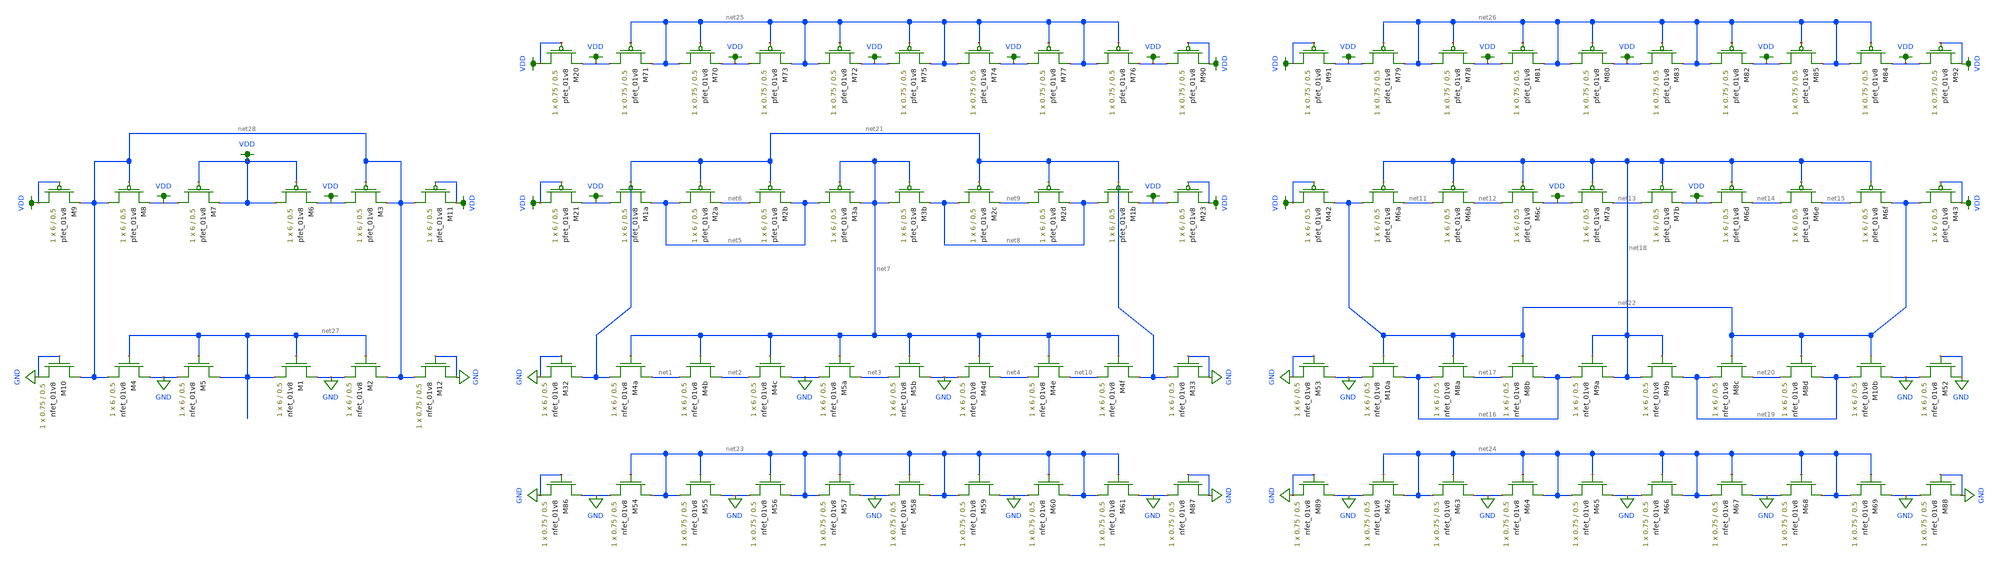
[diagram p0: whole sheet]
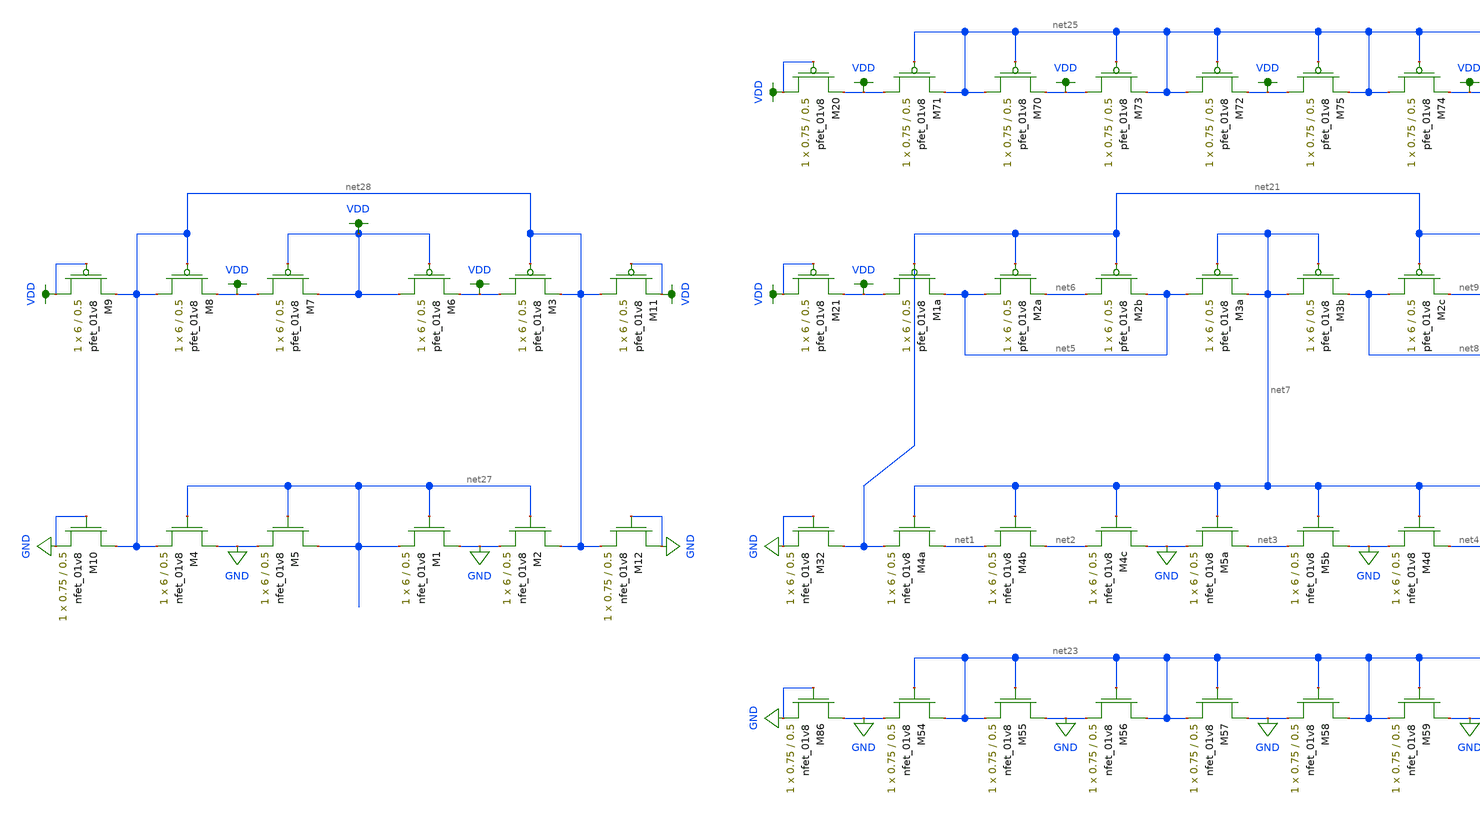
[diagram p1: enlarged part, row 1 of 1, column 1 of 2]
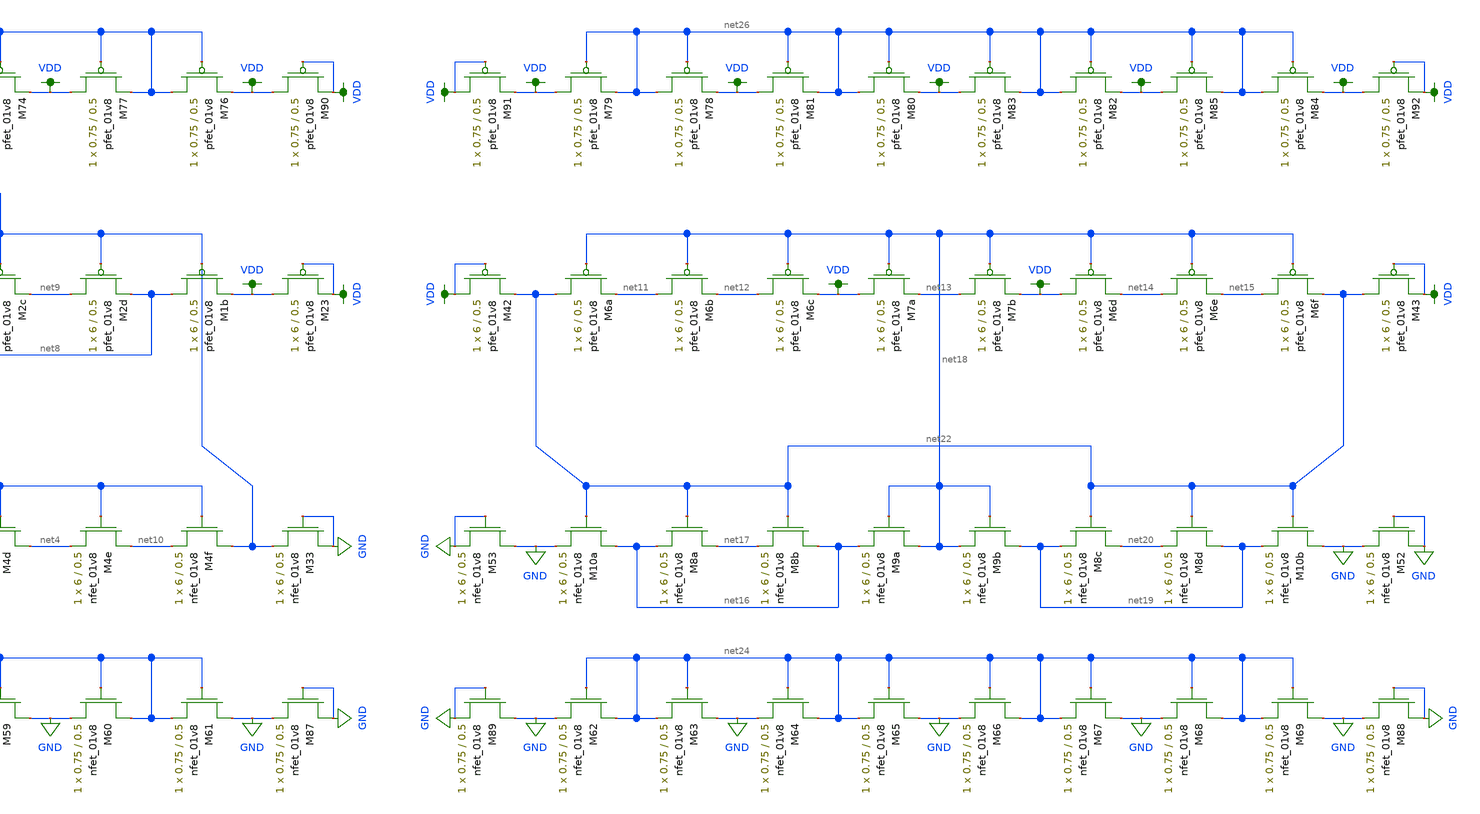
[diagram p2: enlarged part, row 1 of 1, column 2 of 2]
** sch_path: mini3/schem/bias_lvs.sch
**.subckt bias_lvs
XM4a net1 net7 net21 GND sky130_fd_pr__nfet_01v8 L=0.5 W=6 nf=1 ad='int((nf+1)/2) * W/nf * 0.29' as='int((nf+2)/2) * W/nf * 0.29'
+ pd='2*int((nf+1)/2) * (W/nf + 0.29)' ps='2*int((nf+2)/2) * (W/nf + 0.29)' nrd='0.29 / W' nrs='0.29 / W'
+ sa=0 sb=0 sd=0 mult=1 m=1
XM4b net2 net7 net1 GND sky130_fd_pr__nfet_01v8 L=0.5 W=6 nf=1 ad='int((nf+1)/2) * W/nf * 0.29' as='int((nf+2)/2) * W/nf * 0.29'
+ pd='2*int((nf+1)/2) * (W/nf + 0.29)' ps='2*int((nf+2)/2) * (W/nf + 0.29)' nrd='0.29 / W' nrs='0.29 / W'
+ sa=0 sb=0 sd=0 mult=1 m=1
XM4c GND net7 net2 GND sky130_fd_pr__nfet_01v8 L=0.5 W=6 nf=1 ad='int((nf+1)/2) * W/nf * 0.29' as='int((nf+2)/2) * W/nf * 0.29'
+ pd='2*int((nf+1)/2) * (W/nf + 0.29)' ps='2*int((nf+2)/2) * (W/nf + 0.29)' nrd='0.29 / W' nrs='0.29 / W'
+ sa=0 sb=0 sd=0 mult=1 m=1
XM5a net3 net7 GND GND sky130_fd_pr__nfet_01v8 L=0.5 W=6 nf=1 ad='int((nf+1)/2) * W/nf * 0.29' as='int((nf+2)/2) * W/nf * 0.29'
+ pd='2*int((nf+1)/2) * (W/nf + 0.29)' ps='2*int((nf+2)/2) * (W/nf + 0.29)' nrd='0.29 / W' nrs='0.29 / W'
+ sa=0 sb=0 sd=0 mult=1 m=1
XM5b GND net7 net3 GND sky130_fd_pr__nfet_01v8 L=0.5 W=6 nf=1 ad='int((nf+1)/2) * W/nf * 0.29' as='int((nf+2)/2) * W/nf * 0.29'
+ pd='2*int((nf+1)/2) * (W/nf + 0.29)' ps='2*int((nf+2)/2) * (W/nf + 0.29)' nrd='0.29 / W' nrs='0.29 / W'
+ sa=0 sb=0 sd=0 mult=1 m=1
XM4d net4 net7 GND GND sky130_fd_pr__nfet_01v8 L=0.5 W=6 nf=1 ad='int((nf+1)/2) * W/nf * 0.29' as='int((nf+2)/2) * W/nf * 0.29'
+ pd='2*int((nf+1)/2) * (W/nf + 0.29)' ps='2*int((nf+2)/2) * (W/nf + 0.29)' nrd='0.29 / W' nrs='0.29 / W'
+ sa=0 sb=0 sd=0 mult=1 m=1
XM4e net10 net7 net4 GND sky130_fd_pr__nfet_01v8 L=0.5 W=6 nf=1 ad='int((nf+1)/2) * W/nf * 0.29' as='int((nf+2)/2) * W/nf * 0.29'
+ pd='2*int((nf+1)/2) * (W/nf + 0.29)' ps='2*int((nf+2)/2) * (W/nf + 0.29)' nrd='0.29 / W' nrs='0.29 / W'
+ sa=0 sb=0 sd=0 mult=1 m=1
XM4f net21 net7 net10 GND sky130_fd_pr__nfet_01v8 L=0.5 W=6 nf=1 ad='int((nf+1)/2) * W/nf * 0.29' as='int((nf+2)/2) * W/nf * 0.29'
+ pd='2*int((nf+1)/2) * (W/nf + 0.29)' ps='2*int((nf+2)/2) * (W/nf + 0.29)' nrd='0.29 / W' nrs='0.29 / W'
+ sa=0 sb=0 sd=0 mult=1 m=1
XM1a VDD net21 net5 VDD sky130_fd_pr__pfet_01v8 L=0.5 W=6 nf=1 ad='int((nf+1)/2) * W/nf * 0.29' as='int((nf+2)/2) * W/nf * 0.29'
+ pd='2*int((nf+1)/2) * (W/nf + 0.29)' ps='2*int((nf+2)/2) * (W/nf + 0.29)' nrd='0.29 / W' nrs='0.29 / W'
+ sa=0 sb=0 sd=0 mult=1 m=1
XM2a net5 net21 net6 VDD sky130_fd_pr__pfet_01v8 L=0.5 W=6 nf=1 ad='int((nf+1)/2) * W/nf * 0.29' as='int((nf+2)/2) * W/nf * 0.29'
+ pd='2*int((nf+1)/2) * (W/nf + 0.29)' ps='2*int((nf+2)/2) * (W/nf + 0.29)' nrd='0.29 / W' nrs='0.29 / W'
+ sa=0 sb=0 sd=0 mult=1 m=1
XM2b net6 net21 net5 VDD sky130_fd_pr__pfet_01v8 L=0.5 W=6 nf=1 ad='int((nf+1)/2) * W/nf * 0.29' as='int((nf+2)/2) * W/nf * 0.29'
+ pd='2*int((nf+1)/2) * (W/nf + 0.29)' ps='2*int((nf+2)/2) * (W/nf + 0.29)' nrd='0.29 / W' nrs='0.29 / W'
+ sa=0 sb=0 sd=0 mult=1 m=1
XM3a net5 net7 net7 VDD sky130_fd_pr__pfet_01v8 L=0.5 W=6 nf=1 ad='int((nf+1)/2) * W/nf * 0.29' as='int((nf+2)/2) * W/nf * 0.29'
+ pd='2*int((nf+1)/2) * (W/nf + 0.29)' ps='2*int((nf+2)/2) * (W/nf + 0.29)' nrd='0.29 / W' nrs='0.29 / W'
+ sa=0 sb=0 sd=0 mult=1 m=1
XM3b net7 net7 net8 VDD sky130_fd_pr__pfet_01v8 L=0.5 W=6 nf=1 ad='int((nf+1)/2) * W/nf * 0.29' as='int((nf+2)/2) * W/nf * 0.29'
+ pd='2*int((nf+1)/2) * (W/nf + 0.29)' ps='2*int((nf+2)/2) * (W/nf + 0.29)' nrd='0.29 / W' nrs='0.29 / W'
+ sa=0 sb=0 sd=0 mult=1 m=1
XM2c net8 net21 net9 VDD sky130_fd_pr__pfet_01v8 L=0.5 W=6 nf=1 ad='int((nf+1)/2) * W/nf * 0.29' as='int((nf+2)/2) * W/nf * 0.29'
+ pd='2*int((nf+1)/2) * (W/nf + 0.29)' ps='2*int((nf+2)/2) * (W/nf + 0.29)' nrd='0.29 / W' nrs='0.29 / W'
+ sa=0 sb=0 sd=0 mult=1 m=1
XM2d net9 net21 net8 VDD sky130_fd_pr__pfet_01v8 L=0.5 W=6 nf=1 ad='int((nf+1)/2) * W/nf * 0.29' as='int((nf+2)/2) * W/nf * 0.29'
+ pd='2*int((nf+1)/2) * (W/nf + 0.29)' ps='2*int((nf+2)/2) * (W/nf + 0.29)' nrd='0.29 / W' nrs='0.29 / W'
+ sa=0 sb=0 sd=0 mult=1 m=1
XM1b net8 net21 VDD VDD sky130_fd_pr__pfet_01v8 L=0.5 W=6 nf=1 ad='int((nf+1)/2) * W/nf * 0.29' as='int((nf+2)/2) * W/nf * 0.29'
+ pd='2*int((nf+1)/2) * (W/nf + 0.29)' ps='2*int((nf+2)/2) * (W/nf + 0.29)' nrd='0.29 / W' nrs='0.29 / W'
+ sa=0 sb=0 sd=0 mult=1 m=1
XM6a net22 net18 net11 VDD sky130_fd_pr__pfet_01v8 L=0.5 W=6 nf=1 ad='int((nf+1)/2) * W/nf * 0.29' as='int((nf+2)/2) * W/nf * 0.29'
+ pd='2*int((nf+1)/2) * (W/nf + 0.29)' ps='2*int((nf+2)/2) * (W/nf + 0.29)' nrd='0.29 / W' nrs='0.29 / W'
+ sa=0 sb=0 sd=0 mult=1 m=1
XM6b net11 net18 net12 VDD sky130_fd_pr__pfet_01v8 L=0.5 W=6 nf=1 ad='int((nf+1)/2) * W/nf * 0.29' as='int((nf+2)/2) * W/nf * 0.29'
+ pd='2*int((nf+1)/2) * (W/nf + 0.29)' ps='2*int((nf+2)/2) * (W/nf + 0.29)' nrd='0.29 / W' nrs='0.29 / W'
+ sa=0 sb=0 sd=0 mult=1 m=1
XM6c net12 net18 VDD VDD sky130_fd_pr__pfet_01v8 L=0.5 W=6 nf=1 ad='int((nf+1)/2) * W/nf * 0.29' as='int((nf+2)/2) * W/nf * 0.29'
+ pd='2*int((nf+1)/2) * (W/nf + 0.29)' ps='2*int((nf+2)/2) * (W/nf + 0.29)' nrd='0.29 / W' nrs='0.29 / W'
+ sa=0 sb=0 sd=0 mult=1 m=1
XM7a VDD net18 net13 VDD sky130_fd_pr__pfet_01v8 L=0.5 W=6 nf=1 ad='int((nf+1)/2) * W/nf * 0.29' as='int((nf+2)/2) * W/nf * 0.29'
+ pd='2*int((nf+1)/2) * (W/nf + 0.29)' ps='2*int((nf+2)/2) * (W/nf + 0.29)' nrd='0.29 / W' nrs='0.29 / W'
+ sa=0 sb=0 sd=0 mult=1 m=1
XM7b net13 net18 VDD VDD sky130_fd_pr__pfet_01v8 L=0.5 W=6 nf=1 ad='int((nf+1)/2) * W/nf * 0.29' as='int((nf+2)/2) * W/nf * 0.29'
+ pd='2*int((nf+1)/2) * (W/nf + 0.29)' ps='2*int((nf+2)/2) * (W/nf + 0.29)' nrd='0.29 / W' nrs='0.29 / W'
+ sa=0 sb=0 sd=0 mult=1 m=1
XM6d VDD net18 net14 VDD sky130_fd_pr__pfet_01v8 L=0.5 W=6 nf=1 ad='int((nf+1)/2) * W/nf * 0.29' as='int((nf+2)/2) * W/nf * 0.29'
+ pd='2*int((nf+1)/2) * (W/nf + 0.29)' ps='2*int((nf+2)/2) * (W/nf + 0.29)' nrd='0.29 / W' nrs='0.29 / W'
+ sa=0 sb=0 sd=0 mult=1 m=1
XM6e net14 net18 net15 VDD sky130_fd_pr__pfet_01v8 L=0.5 W=6 nf=1 ad='int((nf+1)/2) * W/nf * 0.29' as='int((nf+2)/2) * W/nf * 0.29'
+ pd='2*int((nf+1)/2) * (W/nf + 0.29)' ps='2*int((nf+2)/2) * (W/nf + 0.29)' nrd='0.29 / W' nrs='0.29 / W'
+ sa=0 sb=0 sd=0 mult=1 m=1
XM6f net15 net18 net22 VDD sky130_fd_pr__pfet_01v8 L=0.5 W=6 nf=1 ad='int((nf+1)/2) * W/nf * 0.29' as='int((nf+2)/2) * W/nf * 0.29'
+ pd='2*int((nf+1)/2) * (W/nf + 0.29)' ps='2*int((nf+2)/2) * (W/nf + 0.29)' nrd='0.29 / W' nrs='0.29 / W'
+ sa=0 sb=0 sd=0 mult=1 m=1
XM10a net16 net22 GND GND sky130_fd_pr__nfet_01v8 L=0.5 W=6 nf=1 ad='int((nf+1)/2) * W/nf * 0.29' as='int((nf+2)/2) * W/nf * 0.29'
+ pd='2*int((nf+1)/2) * (W/nf + 0.29)' ps='2*int((nf+2)/2) * (W/nf + 0.29)' nrd='0.29 / W' nrs='0.29 / W'
+ sa=0 sb=0 sd=0 mult=1 m=1
XM8a net17 net22 net16 GND sky130_fd_pr__nfet_01v8 L=0.5 W=6 nf=1 ad='int((nf+1)/2) * W/nf * 0.29' as='int((nf+2)/2) * W/nf * 0.29'
+ pd='2*int((nf+1)/2) * (W/nf + 0.29)' ps='2*int((nf+2)/2) * (W/nf + 0.29)' nrd='0.29 / W' nrs='0.29 / W'
+ sa=0 sb=0 sd=0 mult=1 m=1
XM8b net16 net22 net17 GND sky130_fd_pr__nfet_01v8 L=0.5 W=6 nf=1 ad='int((nf+1)/2) * W/nf * 0.29' as='int((nf+2)/2) * W/nf * 0.29'
+ pd='2*int((nf+1)/2) * (W/nf + 0.29)' ps='2*int((nf+2)/2) * (W/nf + 0.29)' nrd='0.29 / W' nrs='0.29 / W'
+ sa=0 sb=0 sd=0 mult=1 m=1
XM9a net18 net18 net16 GND sky130_fd_pr__nfet_01v8 L=0.5 W=6 nf=1 ad='int((nf+1)/2) * W/nf * 0.29' as='int((nf+2)/2) * W/nf * 0.29'
+ pd='2*int((nf+1)/2) * (W/nf + 0.29)' ps='2*int((nf+2)/2) * (W/nf + 0.29)' nrd='0.29 / W' nrs='0.29 / W'
+ sa=0 sb=0 sd=0 mult=1 m=1
XM9b net19 net18 net18 GND sky130_fd_pr__nfet_01v8 L=0.5 W=6 nf=1 ad='int((nf+1)/2) * W/nf * 0.29' as='int((nf+2)/2) * W/nf * 0.29'
+ pd='2*int((nf+1)/2) * (W/nf + 0.29)' ps='2*int((nf+2)/2) * (W/nf + 0.29)' nrd='0.29 / W' nrs='0.29 / W'
+ sa=0 sb=0 sd=0 mult=1 m=1
XM8c net20 net22 net19 GND sky130_fd_pr__nfet_01v8 L=0.5 W=6 nf=1 ad='int((nf+1)/2) * W/nf * 0.29' as='int((nf+2)/2) * W/nf * 0.29'
+ pd='2*int((nf+1)/2) * (W/nf + 0.29)' ps='2*int((nf+2)/2) * (W/nf + 0.29)' nrd='0.29 / W' nrs='0.29 / W'
+ sa=0 sb=0 sd=0 mult=1 m=1
XM8d net19 net22 net20 GND sky130_fd_pr__nfet_01v8 L=0.5 W=6 nf=1 ad='int((nf+1)/2) * W/nf * 0.29' as='int((nf+2)/2) * W/nf * 0.29'
+ pd='2*int((nf+1)/2) * (W/nf + 0.29)' ps='2*int((nf+2)/2) * (W/nf + 0.29)' nrd='0.29 / W' nrs='0.29 / W'
+ sa=0 sb=0 sd=0 mult=1 m=1
XM10b GND net22 net19 GND sky130_fd_pr__nfet_01v8 L=0.5 W=6 nf=1 ad='int((nf+1)/2) * W/nf * 0.29' as='int((nf+2)/2) * W/nf * 0.29'
+ pd='2*int((nf+1)/2) * (W/nf + 0.29)' ps='2*int((nf+2)/2) * (W/nf + 0.29)' nrd='0.29 / W' nrs='0.29 / W'
+ sa=0 sb=0 sd=0 mult=1 m=1
XM23 VDD VDD VDD VDD sky130_fd_pr__pfet_01v8 L=0.5 W=6 nf=1 ad='int((nf+1)/2) * W/nf * 0.29' as='int((nf+2)/2) * W/nf * 0.29'
+ pd='2*int((nf+1)/2) * (W/nf + 0.29)' ps='2*int((nf+2)/2) * (W/nf + 0.29)' nrd='0.29 / W' nrs='0.29 / W'
+ sa=0 sb=0 sd=0 mult=1 m=1
XM32 net21 GND GND GND sky130_fd_pr__nfet_01v8 L=0.5 W=6 nf=1 ad='int((nf+1)/2) * W/nf * 0.29' as='int((nf+2)/2) * W/nf * 0.29'
+ pd='2*int((nf+1)/2) * (W/nf + 0.29)' ps='2*int((nf+2)/2) * (W/nf + 0.29)' nrd='0.29 / W' nrs='0.29 / W'
+ sa=0 sb=0 sd=0 mult=1 m=1
XM33 GND GND net21 GND sky130_fd_pr__nfet_01v8 L=0.5 W=6 nf=1 ad='int((nf+1)/2) * W/nf * 0.29' as='int((nf+2)/2) * W/nf * 0.29'
+ pd='2*int((nf+1)/2) * (W/nf + 0.29)' ps='2*int((nf+2)/2) * (W/nf + 0.29)' nrd='0.29 / W' nrs='0.29 / W'
+ sa=0 sb=0 sd=0 mult=1 m=1
XM42 VDD VDD net22 VDD sky130_fd_pr__pfet_01v8 L=0.5 W=6 nf=1 ad='int((nf+1)/2) * W/nf * 0.29' as='int((nf+2)/2) * W/nf * 0.29'
+ pd='2*int((nf+1)/2) * (W/nf + 0.29)' ps='2*int((nf+2)/2) * (W/nf + 0.29)' nrd='0.29 / W' nrs='0.29 / W'
+ sa=0 sb=0 sd=0 mult=1 m=1
XM43 net22 VDD VDD VDD sky130_fd_pr__pfet_01v8 L=0.5 W=6 nf=1 ad='int((nf+1)/2) * W/nf * 0.29' as='int((nf+2)/2) * W/nf * 0.29'
+ pd='2*int((nf+1)/2) * (W/nf + 0.29)' ps='2*int((nf+2)/2) * (W/nf + 0.29)' nrd='0.29 / W' nrs='0.29 / W'
+ sa=0 sb=0 sd=0 mult=1 m=1
XM52 GND GND GND GND sky130_fd_pr__nfet_01v8 L=0.5 W=6 nf=1 ad='int((nf+1)/2) * W/nf * 0.29' as='int((nf+2)/2) * W/nf * 0.29'
+ pd='2*int((nf+1)/2) * (W/nf + 0.29)' ps='2*int((nf+2)/2) * (W/nf + 0.29)' nrd='0.29 / W' nrs='0.29 / W'
+ sa=0 sb=0 sd=0 mult=1 m=1
XM53 GND GND GND GND sky130_fd_pr__nfet_01v8 L=0.5 W=6 nf=1 ad='int((nf+1)/2) * W/nf * 0.29' as='int((nf+2)/2) * W/nf * 0.29'
+ pd='2*int((nf+1)/2) * (W/nf + 0.29)' ps='2*int((nf+2)/2) * (W/nf + 0.29)' nrd='0.29 / W' nrs='0.29 / W'
+ sa=0 sb=0 sd=0 mult=1 m=1
XM54 net23 net23 GND GND sky130_fd_pr__nfet_01v8 L=0.5 W=0.75 nf=1 ad='int((nf+1)/2) * W/nf * 0.29' as='int((nf+2)/2) * W/nf * 0.29'
+ pd='2*int((nf+1)/2) * (W/nf + 0.29)' ps='2*int((nf+2)/2) * (W/nf + 0.29)' nrd='0.29 / W' nrs='0.29 / W'
+ sa=0 sb=0 sd=0 mult=1 m=1
XM55 GND net23 net23 GND sky130_fd_pr__nfet_01v8 L=0.5 W=0.75 nf=1 ad='int((nf+1)/2) * W/nf * 0.29' as='int((nf+2)/2) * W/nf * 0.29'
+ pd='2*int((nf+1)/2) * (W/nf + 0.29)' ps='2*int((nf+2)/2) * (W/nf + 0.29)' nrd='0.29 / W' nrs='0.29 / W'
+ sa=0 sb=0 sd=0 mult=1 m=1
XM56 net23 net23 GND GND sky130_fd_pr__nfet_01v8 L=0.5 W=0.75 nf=1 ad='int((nf+1)/2) * W/nf * 0.29' as='int((nf+2)/2) * W/nf * 0.29'
+ pd='2*int((nf+1)/2) * (W/nf + 0.29)' ps='2*int((nf+2)/2) * (W/nf + 0.29)' nrd='0.29 / W' nrs='0.29 / W'
+ sa=0 sb=0 sd=0 mult=1 m=1
XM57 GND net23 net23 GND sky130_fd_pr__nfet_01v8 L=0.5 W=0.75 nf=1 ad='int((nf+1)/2) * W/nf * 0.29' as='int((nf+2)/2) * W/nf * 0.29'
+ pd='2*int((nf+1)/2) * (W/nf + 0.29)' ps='2*int((nf+2)/2) * (W/nf + 0.29)' nrd='0.29 / W' nrs='0.29 / W'
+ sa=0 sb=0 sd=0 mult=1 m=1
XM58 net23 net23 GND GND sky130_fd_pr__nfet_01v8 L=0.5 W=0.75 nf=1 ad='int((nf+1)/2) * W/nf * 0.29' as='int((nf+2)/2) * W/nf * 0.29'
+ pd='2*int((nf+1)/2) * (W/nf + 0.29)' ps='2*int((nf+2)/2) * (W/nf + 0.29)' nrd='0.29 / W' nrs='0.29 / W'
+ sa=0 sb=0 sd=0 mult=1 m=1
XM59 GND net23 net23 GND sky130_fd_pr__nfet_01v8 L=0.5 W=0.75 nf=1 ad='int((nf+1)/2) * W/nf * 0.29' as='int((nf+2)/2) * W/nf * 0.29'
+ pd='2*int((nf+1)/2) * (W/nf + 0.29)' ps='2*int((nf+2)/2) * (W/nf + 0.29)' nrd='0.29 / W' nrs='0.29 / W'
+ sa=0 sb=0 sd=0 mult=1 m=1
XM60 net23 net23 GND GND sky130_fd_pr__nfet_01v8 L=0.5 W=0.75 nf=1 ad='int((nf+1)/2) * W/nf * 0.29' as='int((nf+2)/2) * W/nf * 0.29'
+ pd='2*int((nf+1)/2) * (W/nf + 0.29)' ps='2*int((nf+2)/2) * (W/nf + 0.29)' nrd='0.29 / W' nrs='0.29 / W'
+ sa=0 sb=0 sd=0 mult=1 m=1
XM61 GND net23 net23 GND sky130_fd_pr__nfet_01v8 L=0.5 W=0.75 nf=1 ad='int((nf+1)/2) * W/nf * 0.29' as='int((nf+2)/2) * W/nf * 0.29'
+ pd='2*int((nf+1)/2) * (W/nf + 0.29)' ps='2*int((nf+2)/2) * (W/nf + 0.29)' nrd='0.29 / W' nrs='0.29 / W'
+ sa=0 sb=0 sd=0 mult=1 m=1
XM62 net24 net24 GND GND sky130_fd_pr__nfet_01v8 L=0.5 W=0.75 nf=1 ad='int((nf+1)/2) * W/nf * 0.29' as='int((nf+2)/2) * W/nf * 0.29'
+ pd='2*int((nf+1)/2) * (W/nf + 0.29)' ps='2*int((nf+2)/2) * (W/nf + 0.29)' nrd='0.29 / W' nrs='0.29 / W'
+ sa=0 sb=0 sd=0 mult=1 m=1
XM63 GND net24 net24 GND sky130_fd_pr__nfet_01v8 L=0.5 W=0.75 nf=1 ad='int((nf+1)/2) * W/nf * 0.29' as='int((nf+2)/2) * W/nf * 0.29'
+ pd='2*int((nf+1)/2) * (W/nf + 0.29)' ps='2*int((nf+2)/2) * (W/nf + 0.29)' nrd='0.29 / W' nrs='0.29 / W'
+ sa=0 sb=0 sd=0 mult=1 m=1
XM64 net24 net24 GND GND sky130_fd_pr__nfet_01v8 L=0.5 W=0.75 nf=1 ad='int((nf+1)/2) * W/nf * 0.29' as='int((nf+2)/2) * W/nf * 0.29'
+ pd='2*int((nf+1)/2) * (W/nf + 0.29)' ps='2*int((nf+2)/2) * (W/nf + 0.29)' nrd='0.29 / W' nrs='0.29 / W'
+ sa=0 sb=0 sd=0 mult=1 m=1
XM65 GND net24 net24 GND sky130_fd_pr__nfet_01v8 L=0.5 W=0.75 nf=1 ad='int((nf+1)/2) * W/nf * 0.29' as='int((nf+2)/2) * W/nf * 0.29'
+ pd='2*int((nf+1)/2) * (W/nf + 0.29)' ps='2*int((nf+2)/2) * (W/nf + 0.29)' nrd='0.29 / W' nrs='0.29 / W'
+ sa=0 sb=0 sd=0 mult=1 m=1
XM66 net24 net24 GND GND sky130_fd_pr__nfet_01v8 L=0.5 W=0.75 nf=1 ad='int((nf+1)/2) * W/nf * 0.29' as='int((nf+2)/2) * W/nf * 0.29'
+ pd='2*int((nf+1)/2) * (W/nf + 0.29)' ps='2*int((nf+2)/2) * (W/nf + 0.29)' nrd='0.29 / W' nrs='0.29 / W'
+ sa=0 sb=0 sd=0 mult=1 m=1
XM67 GND net24 net24 GND sky130_fd_pr__nfet_01v8 L=0.5 W=0.75 nf=1 ad='int((nf+1)/2) * W/nf * 0.29' as='int((nf+2)/2) * W/nf * 0.29'
+ pd='2*int((nf+1)/2) * (W/nf + 0.29)' ps='2*int((nf+2)/2) * (W/nf + 0.29)' nrd='0.29 / W' nrs='0.29 / W'
+ sa=0 sb=0 sd=0 mult=1 m=1
XM68 net24 net24 GND GND sky130_fd_pr__nfet_01v8 L=0.5 W=0.75 nf=1 ad='int((nf+1)/2) * W/nf * 0.29' as='int((nf+2)/2) * W/nf * 0.29'
+ pd='2*int((nf+1)/2) * (W/nf + 0.29)' ps='2*int((nf+2)/2) * (W/nf + 0.29)' nrd='0.29 / W' nrs='0.29 / W'
+ sa=0 sb=0 sd=0 mult=1 m=1
XM69 GND net24 net24 GND sky130_fd_pr__nfet_01v8 L=0.5 W=0.75 nf=1 ad='int((nf+1)/2) * W/nf * 0.29' as='int((nf+2)/2) * W/nf * 0.29'
+ pd='2*int((nf+1)/2) * (W/nf + 0.29)' ps='2*int((nf+2)/2) * (W/nf + 0.29)' nrd='0.29 / W' nrs='0.29 / W'
+ sa=0 sb=0 sd=0 mult=1 m=1
XM70 net25 net25 VDD VDD sky130_fd_pr__pfet_01v8 L=0.5 W=0.75 nf=1 ad='int((nf+1)/2) * W/nf * 0.29' as='int((nf+2)/2) * W/nf * 0.29'
+ pd='2*int((nf+1)/2) * (W/nf + 0.29)' ps='2*int((nf+2)/2) * (W/nf + 0.29)' nrd='0.29 / W' nrs='0.29 / W'
+ sa=0 sb=0 sd=0 mult=1 m=1
XM71 VDD net25 net25 VDD sky130_fd_pr__pfet_01v8 L=0.5 W=0.75 nf=1 ad='int((nf+1)/2) * W/nf * 0.29' as='int((nf+2)/2) * W/nf * 0.29'
+ pd='2*int((nf+1)/2) * (W/nf + 0.29)' ps='2*int((nf+2)/2) * (W/nf + 0.29)' nrd='0.29 / W' nrs='0.29 / W'
+ sa=0 sb=0 sd=0 mult=1 m=1
XM72 net25 net25 VDD VDD sky130_fd_pr__pfet_01v8 L=0.5 W=0.75 nf=1 ad='int((nf+1)/2) * W/nf * 0.29' as='int((nf+2)/2) * W/nf * 0.29'
+ pd='2*int((nf+1)/2) * (W/nf + 0.29)' ps='2*int((nf+2)/2) * (W/nf + 0.29)' nrd='0.29 / W' nrs='0.29 / W'
+ sa=0 sb=0 sd=0 mult=1 m=1
XM73 VDD net25 net25 VDD sky130_fd_pr__pfet_01v8 L=0.5 W=0.75 nf=1 ad='int((nf+1)/2) * W/nf * 0.29' as='int((nf+2)/2) * W/nf * 0.29'
+ pd='2*int((nf+1)/2) * (W/nf + 0.29)' ps='2*int((nf+2)/2) * (W/nf + 0.29)' nrd='0.29 / W' nrs='0.29 / W'
+ sa=0 sb=0 sd=0 mult=1 m=1
XM74 net25 net25 VDD VDD sky130_fd_pr__pfet_01v8 L=0.5 W=0.75 nf=1 ad='int((nf+1)/2) * W/nf * 0.29' as='int((nf+2)/2) * W/nf * 0.29'
+ pd='2*int((nf+1)/2) * (W/nf + 0.29)' ps='2*int((nf+2)/2) * (W/nf + 0.29)' nrd='0.29 / W' nrs='0.29 / W'
+ sa=0 sb=0 sd=0 mult=1 m=1
XM75 VDD net25 net25 VDD sky130_fd_pr__pfet_01v8 L=0.5 W=0.75 nf=1 ad='int((nf+1)/2) * W/nf * 0.29' as='int((nf+2)/2) * W/nf * 0.29'
+ pd='2*int((nf+1)/2) * (W/nf + 0.29)' ps='2*int((nf+2)/2) * (W/nf + 0.29)' nrd='0.29 / W' nrs='0.29 / W'
+ sa=0 sb=0 sd=0 mult=1 m=1
XM76 net25 net25 VDD VDD sky130_fd_pr__pfet_01v8 L=0.5 W=0.75 nf=1 ad='int((nf+1)/2) * W/nf * 0.29' as='int((nf+2)/2) * W/nf * 0.29'
+ pd='2*int((nf+1)/2) * (W/nf + 0.29)' ps='2*int((nf+2)/2) * (W/nf + 0.29)' nrd='0.29 / W' nrs='0.29 / W'
+ sa=0 sb=0 sd=0 mult=1 m=1
XM77 VDD net25 net25 VDD sky130_fd_pr__pfet_01v8 L=0.5 W=0.75 nf=1 ad='int((nf+1)/2) * W/nf * 0.29' as='int((nf+2)/2) * W/nf * 0.29'
+ pd='2*int((nf+1)/2) * (W/nf + 0.29)' ps='2*int((nf+2)/2) * (W/nf + 0.29)' nrd='0.29 / W' nrs='0.29 / W'
+ sa=0 sb=0 sd=0 mult=1 m=1
XM78 net26 net26 VDD VDD sky130_fd_pr__pfet_01v8 L=0.5 W=0.75 nf=1 ad='int((nf+1)/2) * W/nf * 0.29' as='int((nf+2)/2) * W/nf * 0.29'
+ pd='2*int((nf+1)/2) * (W/nf + 0.29)' ps='2*int((nf+2)/2) * (W/nf + 0.29)' nrd='0.29 / W' nrs='0.29 / W'
+ sa=0 sb=0 sd=0 mult=1 m=1
XM79 VDD net26 net26 VDD sky130_fd_pr__pfet_01v8 L=0.5 W=0.75 nf=1 ad='int((nf+1)/2) * W/nf * 0.29' as='int((nf+2)/2) * W/nf * 0.29'
+ pd='2*int((nf+1)/2) * (W/nf + 0.29)' ps='2*int((nf+2)/2) * (W/nf + 0.29)' nrd='0.29 / W' nrs='0.29 / W'
+ sa=0 sb=0 sd=0 mult=1 m=1
XM80 net26 net26 VDD VDD sky130_fd_pr__pfet_01v8 L=0.5 W=0.75 nf=1 ad='int((nf+1)/2) * W/nf * 0.29' as='int((nf+2)/2) * W/nf * 0.29'
+ pd='2*int((nf+1)/2) * (W/nf + 0.29)' ps='2*int((nf+2)/2) * (W/nf + 0.29)' nrd='0.29 / W' nrs='0.29 / W'
+ sa=0 sb=0 sd=0 mult=1 m=1
XM81 VDD net26 net26 VDD sky130_fd_pr__pfet_01v8 L=0.5 W=0.75 nf=1 ad='int((nf+1)/2) * W/nf * 0.29' as='int((nf+2)/2) * W/nf * 0.29'
+ pd='2*int((nf+1)/2) * (W/nf + 0.29)' ps='2*int((nf+2)/2) * (W/nf + 0.29)' nrd='0.29 / W' nrs='0.29 / W'
+ sa=0 sb=0 sd=0 mult=1 m=1
XM82 net26 net26 VDD VDD sky130_fd_pr__pfet_01v8 L=0.5 W=0.75 nf=1 ad='int((nf+1)/2) * W/nf * 0.29' as='int((nf+2)/2) * W/nf * 0.29'
+ pd='2*int((nf+1)/2) * (W/nf + 0.29)' ps='2*int((nf+2)/2) * (W/nf + 0.29)' nrd='0.29 / W' nrs='0.29 / W'
+ sa=0 sb=0 sd=0 mult=1 m=1
XM83 VDD net26 net26 VDD sky130_fd_pr__pfet_01v8 L=0.5 W=0.75 nf=1 ad='int((nf+1)/2) * W/nf * 0.29' as='int((nf+2)/2) * W/nf * 0.29'
+ pd='2*int((nf+1)/2) * (W/nf + 0.29)' ps='2*int((nf+2)/2) * (W/nf + 0.29)' nrd='0.29 / W' nrs='0.29 / W'
+ sa=0 sb=0 sd=0 mult=1 m=1
XM84 net26 net26 VDD VDD sky130_fd_pr__pfet_01v8 L=0.5 W=0.75 nf=1 ad='int((nf+1)/2) * W/nf * 0.29' as='int((nf+2)/2) * W/nf * 0.29'
+ pd='2*int((nf+1)/2) * (W/nf + 0.29)' ps='2*int((nf+2)/2) * (W/nf + 0.29)' nrd='0.29 / W' nrs='0.29 / W'
+ sa=0 sb=0 sd=0 mult=1 m=1
XM85 VDD net26 net26 VDD sky130_fd_pr__pfet_01v8 L=0.5 W=0.75 nf=1 ad='int((nf+1)/2) * W/nf * 0.29' as='int((nf+2)/2) * W/nf * 0.29'
+ pd='2*int((nf+1)/2) * (W/nf + 0.29)' ps='2*int((nf+2)/2) * (W/nf + 0.29)' nrd='0.29 / W' nrs='0.29 / W'
+ sa=0 sb=0 sd=0 mult=1 m=1
XM86 GND GND GND GND sky130_fd_pr__nfet_01v8 L=0.5 W=0.75 nf=1 ad='int((nf+1)/2) * W/nf * 0.29' as='int((nf+2)/2) * W/nf * 0.29'
+ pd='2*int((nf+1)/2) * (W/nf + 0.29)' ps='2*int((nf+2)/2) * (W/nf + 0.29)' nrd='0.29 / W' nrs='0.29 / W'
+ sa=0 sb=0 sd=0 mult=1 m=1
XM87 GND GND GND GND sky130_fd_pr__nfet_01v8 L=0.5 W=0.75 nf=1 ad='int((nf+1)/2) * W/nf * 0.29' as='int((nf+2)/2) * W/nf * 0.29'
+ pd='2*int((nf+1)/2) * (W/nf + 0.29)' ps='2*int((nf+2)/2) * (W/nf + 0.29)' nrd='0.29 / W' nrs='0.29 / W'
+ sa=0 sb=0 sd=0 mult=1 m=1
XM88 GND GND GND GND sky130_fd_pr__nfet_01v8 L=0.5 W=0.75 nf=1 ad='int((nf+1)/2) * W/nf * 0.29' as='int((nf+2)/2) * W/nf * 0.29'
+ pd='2*int((nf+1)/2) * (W/nf + 0.29)' ps='2*int((nf+2)/2) * (W/nf + 0.29)' nrd='0.29 / W' nrs='0.29 / W'
+ sa=0 sb=0 sd=0 mult=1 m=1
XM89 GND GND GND GND sky130_fd_pr__nfet_01v8 L=0.5 W=0.75 nf=1 ad='int((nf+1)/2) * W/nf * 0.29' as='int((nf+2)/2) * W/nf * 0.29'
+ pd='2*int((nf+1)/2) * (W/nf + 0.29)' ps='2*int((nf+2)/2) * (W/nf + 0.29)' nrd='0.29 / W' nrs='0.29 / W'
+ sa=0 sb=0 sd=0 mult=1 m=1
XM90 VDD VDD VDD VDD sky130_fd_pr__pfet_01v8 L=0.5 W=0.75 nf=1 ad='int((nf+1)/2) * W/nf * 0.29' as='int((nf+2)/2) * W/nf * 0.29'
+ pd='2*int((nf+1)/2) * (W/nf + 0.29)' ps='2*int((nf+2)/2) * (W/nf + 0.29)' nrd='0.29 / W' nrs='0.29 / W'
+ sa=0 sb=0 sd=0 mult=1 m=1
XM91 VDD VDD VDD VDD sky130_fd_pr__pfet_01v8 L=0.5 W=0.75 nf=1 ad='int((nf+1)/2) * W/nf * 0.29' as='int((nf+2)/2) * W/nf * 0.29'
+ pd='2*int((nf+1)/2) * (W/nf + 0.29)' ps='2*int((nf+2)/2) * (W/nf + 0.29)' nrd='0.29 / W' nrs='0.29 / W'
+ sa=0 sb=0 sd=0 mult=1 m=1
XM92 VDD VDD VDD VDD sky130_fd_pr__pfet_01v8 L=0.5 W=0.75 nf=1 ad='int((nf+1)/2) * W/nf * 0.29' as='int((nf+2)/2) * W/nf * 0.29'
+ pd='2*int((nf+1)/2) * (W/nf + 0.29)' ps='2*int((nf+2)/2) * (W/nf + 0.29)' nrd='0.29 / W' nrs='0.29 / W'
+ sa=0 sb=0 sd=0 mult=1 m=1
XM20 VDD VDD VDD VDD sky130_fd_pr__pfet_01v8 L=0.5 W=0.75 nf=1 ad='int((nf+1)/2) * W/nf * 0.29' as='int((nf+2)/2) * W/nf * 0.29'
+ pd='2*int((nf+1)/2) * (W/nf + 0.29)' ps='2*int((nf+2)/2) * (W/nf + 0.29)' nrd='0.29 / W' nrs='0.29 / W'
+ sa=0 sb=0 sd=0 mult=1 m=1
XM21 VDD VDD VDD VDD sky130_fd_pr__pfet_01v8 L=0.5 W=6 nf=1 ad='int((nf+1)/2) * W/nf * 0.29' as='int((nf+2)/2) * W/nf * 0.29'
+ pd='2*int((nf+1)/2) * (W/nf + 0.29)' ps='2*int((nf+2)/2) * (W/nf + 0.29)' nrd='0.29 / W' nrs='0.29 / W'
+ sa=0 sb=0 sd=0 mult=1 m=1
XM1 GND net27 net27 GND sky130_fd_pr__nfet_01v8 L=0.5 W=6 nf=1 ad='int((nf+1)/2) * W/nf * 0.29' as='int((nf+2)/2) * W/nf * 0.29'
+ pd='2*int((nf+1)/2) * (W/nf + 0.29)' ps='2*int((nf+2)/2) * (W/nf + 0.29)' nrd='0.29 / W' nrs='0.29 / W'
+ sa=0 sb=0 sd=0 mult=1 m=1
XM2 net28 net27 GND GND sky130_fd_pr__nfet_01v8 L=0.5 W=6 nf=1 ad='int((nf+1)/2) * W/nf * 0.29' as='int((nf+2)/2) * W/nf * 0.29'
+ pd='2*int((nf+1)/2) * (W/nf + 0.29)' ps='2*int((nf+2)/2) * (W/nf + 0.29)' nrd='0.29 / W' nrs='0.29 / W'
+ sa=0 sb=0 sd=0 mult=1 m=1
XM3 VDD net28 net28 VDD sky130_fd_pr__pfet_01v8 L=0.5 W=6 nf=1 ad='int((nf+1)/2) * W/nf * 0.29' as='int((nf+2)/2) * W/nf * 0.29'
+ pd='2*int((nf+1)/2) * (W/nf + 0.29)' ps='2*int((nf+2)/2) * (W/nf + 0.29)' nrd='0.29 / W' nrs='0.29 / W'
+ sa=0 sb=0 sd=0 mult=1 m=1
XM4 GND net27 net28 GND sky130_fd_pr__nfet_01v8 L=0.5 W=6 nf=1 ad='int((nf+1)/2) * W/nf * 0.29' as='int((nf+2)/2) * W/nf * 0.29'
+ pd='2*int((nf+1)/2) * (W/nf + 0.29)' ps='2*int((nf+2)/2) * (W/nf + 0.29)' nrd='0.29 / W' nrs='0.29 / W'
+ sa=0 sb=0 sd=0 mult=1 m=1
XM5 net27 net27 GND GND sky130_fd_pr__nfet_01v8 L=0.5 W=6 nf=1 ad='int((nf+1)/2) * W/nf * 0.29' as='int((nf+2)/2) * W/nf * 0.29'
+ pd='2*int((nf+1)/2) * (W/nf + 0.29)' ps='2*int((nf+2)/2) * (W/nf + 0.29)' nrd='0.29 / W' nrs='0.29 / W'
+ sa=0 sb=0 sd=0 mult=1 m=1
XM6 VDD VDD VDD VDD sky130_fd_pr__pfet_01v8 L=0.5 W=6 nf=1 ad='int((nf+1)/2) * W/nf * 0.29' as='int((nf+2)/2) * W/nf * 0.29'
+ pd='2*int((nf+1)/2) * (W/nf + 0.29)' ps='2*int((nf+2)/2) * (W/nf + 0.29)' nrd='0.29 / W' nrs='0.29 / W'
+ sa=0 sb=0 sd=0 mult=1 m=1
XM7 VDD VDD VDD VDD sky130_fd_pr__pfet_01v8 L=0.5 W=6 nf=1 ad='int((nf+1)/2) * W/nf * 0.29' as='int((nf+2)/2) * W/nf * 0.29'
+ pd='2*int((nf+1)/2) * (W/nf + 0.29)' ps='2*int((nf+2)/2) * (W/nf + 0.29)' nrd='0.29 / W' nrs='0.29 / W'
+ sa=0 sb=0 sd=0 mult=1 m=1
XM8 net28 net28 VDD VDD sky130_fd_pr__pfet_01v8 L=0.5 W=6 nf=1 ad='int((nf+1)/2) * W/nf * 0.29' as='int((nf+2)/2) * W/nf * 0.29'
+ pd='2*int((nf+1)/2) * (W/nf + 0.29)' ps='2*int((nf+2)/2) * (W/nf + 0.29)' nrd='0.29 / W' nrs='0.29 / W'
+ sa=0 sb=0 sd=0 mult=1 m=1
XM9 VDD VDD net28 VDD sky130_fd_pr__pfet_01v8 L=0.5 W=6 nf=1 ad='int((nf+1)/2) * W/nf * 0.29' as='int((nf+2)/2) * W/nf * 0.29'
+ pd='2*int((nf+1)/2) * (W/nf + 0.29)' ps='2*int((nf+2)/2) * (W/nf + 0.29)' nrd='0.29 / W' nrs='0.29 / W'
+ sa=0 sb=0 sd=0 mult=1 m=1
XM10 net28 GND GND GND sky130_fd_pr__nfet_01v8 L=0.5 W=0.75 nf=1 ad='int((nf+1)/2) * W/nf * 0.29' as='int((nf+2)/2) * W/nf * 0.29'
+ pd='2*int((nf+1)/2) * (W/nf + 0.29)' ps='2*int((nf+2)/2) * (W/nf + 0.29)' nrd='0.29 / W' nrs='0.29 / W'
+ sa=0 sb=0 sd=0 mult=1 m=1
XM11 net28 VDD VDD VDD sky130_fd_pr__pfet_01v8 L=0.5 W=6 nf=1 ad='int((nf+1)/2) * W/nf * 0.29' as='int((nf+2)/2) * W/nf * 0.29'
+ pd='2*int((nf+1)/2) * (W/nf + 0.29)' ps='2*int((nf+2)/2) * (W/nf + 0.29)' nrd='0.29 / W' nrs='0.29 / W'
+ sa=0 sb=0 sd=0 mult=1 m=1
XM12 GND GND net28 GND sky130_fd_pr__nfet_01v8 L=0.5 W=0.75 nf=1 ad='int((nf+1)/2) * W/nf * 0.29' as='int((nf+2)/2) * W/nf * 0.29'
+ pd='2*int((nf+1)/2) * (W/nf + 0.29)' ps='2*int((nf+2)/2) * (W/nf + 0.29)' nrd='0.29 / W' nrs='0.29 / W'
+ sa=0 sb=0 sd=0 mult=1 m=1
**.ends
.GLOBAL VDD
.GLOBAL GND
.end
